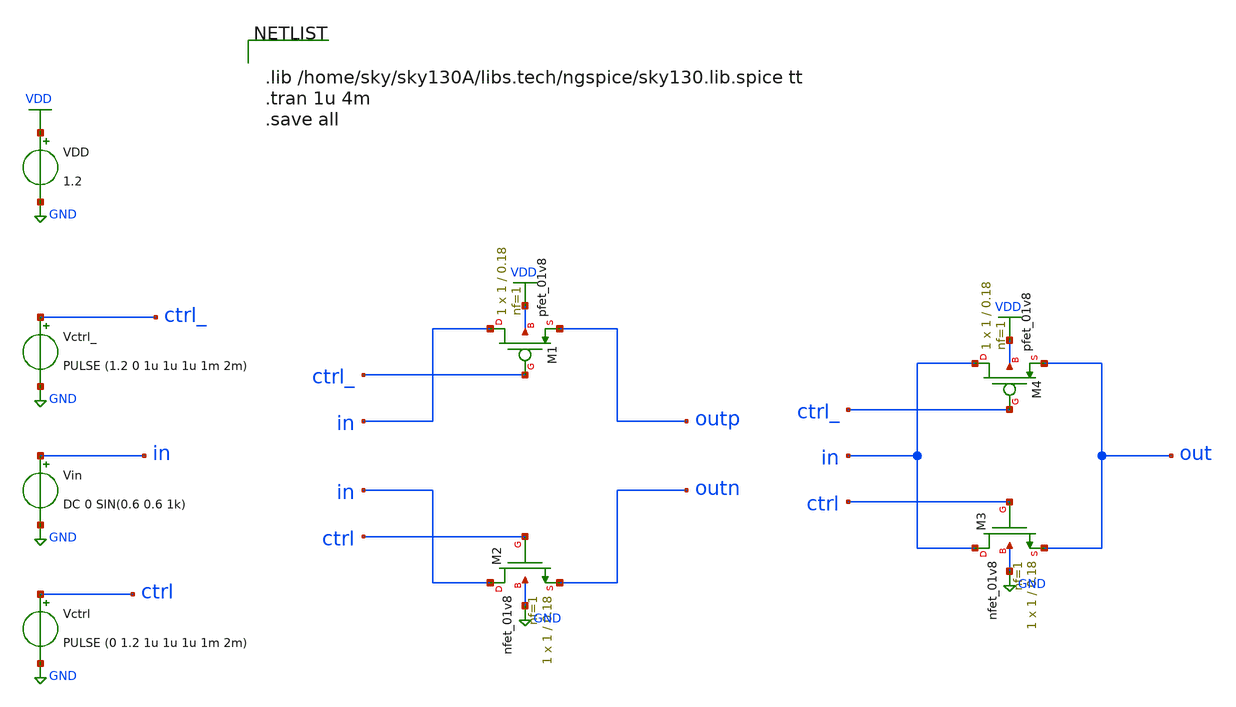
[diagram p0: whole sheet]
** sch_path: xschem/transmission_gate/transmission_gate_vs_single_mos_tb.sch
**.subckt transmission_gate_vs_single_mos_tb
Vin in GND DC 0 SIN(0.6 0.6 1k)
VDD VDD GND 1.2
Vctrl ctrl GND PULSE (0 1.2 1u 1u 1u 1m 2m)
Vctrl_ ctrl_ GND PULSE (1.2 0 1u 1u 1u 1m 2m)
XM3 in ctrl out GND sky130_fd_pr__nfet_01v8 L=0.18 W=1 nf=1 ad='int((nf+1)/2) * W/nf * 0.29' as='int((nf+2)/2) * W/nf * 0.29'
+ pd='2*int((nf+1)/2) * (W/nf + 0.29)' ps='2*int((nf+2)/2) * (W/nf + 0.29)' nrd='0.29 / W' nrs='0.29 / W'
+ sa=0 sb=0 sd=0 mult=1 m=1
XM4 in ctrl_ out VDD sky130_fd_pr__pfet_01v8 L=0.18 W=1 nf=1 ad='int((nf+1)/2) * W/nf * 0.29' as='int((nf+2)/2) * W/nf * 0.29'
+ pd='2*int((nf+1)/2) * (W/nf + 0.29)' ps='2*int((nf+2)/2) * (W/nf + 0.29)' nrd='0.29 / W' nrs='0.29 / W'
+ sa=0 sb=0 sd=0 mult=1 m=1
XM1 in ctrl_ outp VDD sky130_fd_pr__pfet_01v8 L=0.18 W=1 nf=1 ad='int((nf+1)/2) * W/nf * 0.29' as='int((nf+2)/2) * W/nf * 0.29'
+ pd='2*int((nf+1)/2) * (W/nf + 0.29)' ps='2*int((nf+2)/2) * (W/nf + 0.29)' nrd='0.29 / W' nrs='0.29 / W'
+ sa=0 sb=0 sd=0 mult=1 m=1
XM2 in ctrl outn GND sky130_fd_pr__nfet_01v8 L=0.18 W=1 nf=1 ad='int((nf+1)/2) * W/nf * 0.29' as='int((nf+2)/2) * W/nf * 0.29'
+ pd='2*int((nf+1)/2) * (W/nf + 0.29)' ps='2*int((nf+2)/2) * (W/nf + 0.29)' nrd='0.29 / W' nrs='0.29 / W'
+ sa=0 sb=0 sd=0 mult=1 m=1
**** begin user architecture code


.lib /home/sky/sky130A/libs.tech/ngspice/sky130.lib.spice tt
.tran 1u 4m
.save all


**** end user architecture code
**.ends
.GLOBAL VDD
.GLOBAL GND
.end
